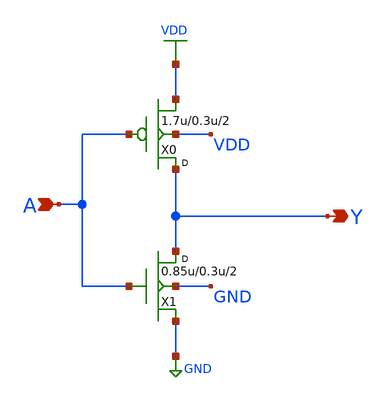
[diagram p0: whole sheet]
** sch_path: lib/12T/xschem/gf180mcu_osu_sc_inv_2.sch
**.subckt gf180mcu_osu_sc_inv_2 A Y
*.ipin A
*.opin Y
X0 Y A VDD VDD pmos_3p3 w=1.7u l=0.3u m=2
X1 Y A GND GND nmos_3p3 w=0.85u l=0.3u m=2
**** begin user architecture code


.inc "/import/yukari1/lrburle/OSU_180/char/techfiles/design.hspice"
.lib "/import/yukari1/lrburle/OSU_180/char/techfiles/sm141064.hspice" typical


**** end user architecture code
**.ends
.GLOBAL VDD
.GLOBAL GND
.end
